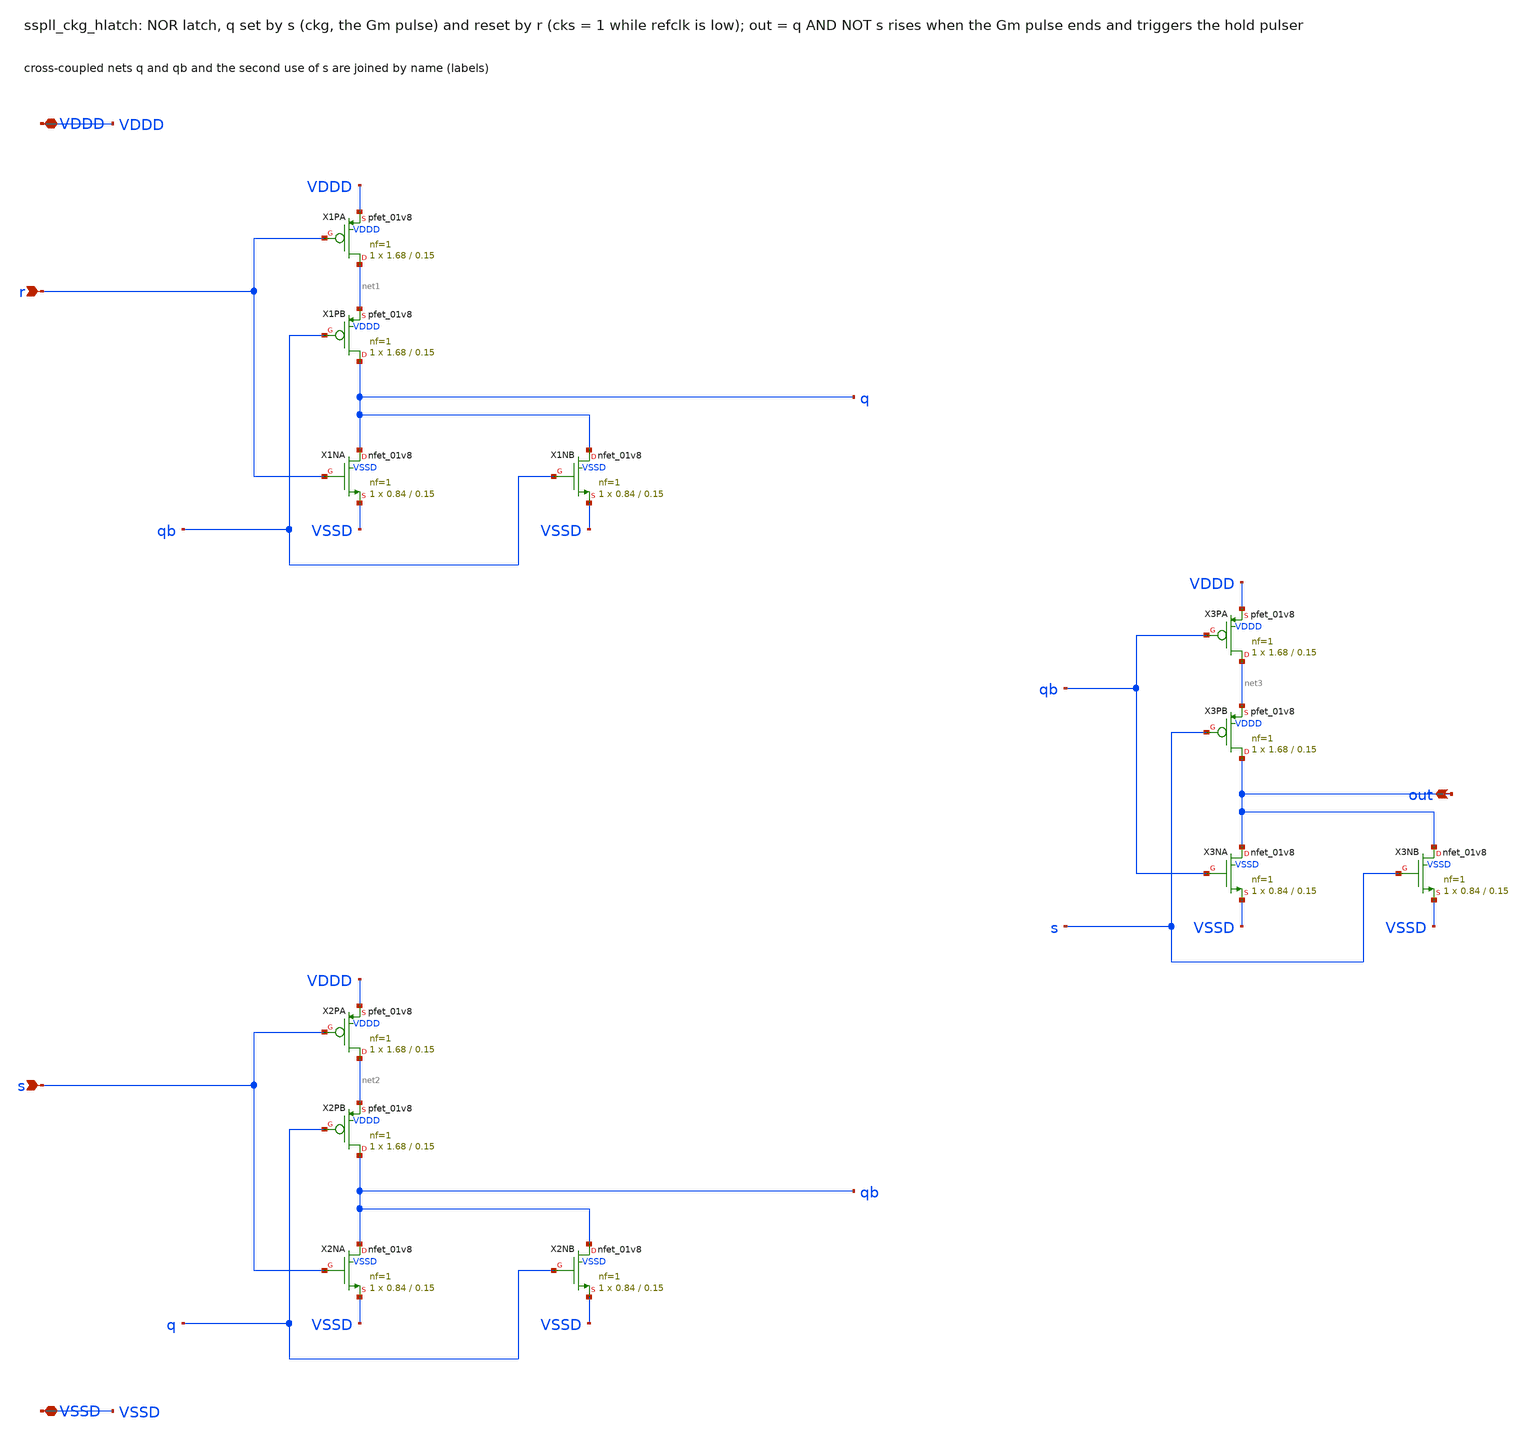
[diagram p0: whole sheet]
** sch_path: xschem/clkgen_hv/sspll_ckg_hlatch.sch
**.subckt sspll_ckg_hlatch r s out VDDD VSSD
*.ipin r
*.ipin s
*.opin out
*.iopin VDDD
*.iopin VSSD
XX1PA net1 r VDDD VDDD sky130_fd_pr__pfet_01v8 L=0.15 W=1.68 nf=1 ad='int((nf+1)/2) * W/nf * 0.29' as='int((nf+2)/2) * W/nf * 0.29'
+ pd='2*int((nf+1)/2) * (W/nf + 0.29)' ps='2*int((nf+2)/2) * (W/nf + 0.29)' nrd='0.29 / W' nrs='0.29 / W'
+ sa=0 sb=0 sd=0 mult=1 m=1
XX1PB q qb net1 VDDD sky130_fd_pr__pfet_01v8 L=0.15 W=1.68 nf=1 ad='int((nf+1)/2) * W/nf * 0.29' as='int((nf+2)/2) * W/nf * 0.29'
+ pd='2*int((nf+1)/2) * (W/nf + 0.29)' ps='2*int((nf+2)/2) * (W/nf + 0.29)' nrd='0.29 / W' nrs='0.29 / W'
+ sa=0 sb=0 sd=0 mult=1 m=1
XX1NA q r VSSD VSSD sky130_fd_pr__nfet_01v8 L=0.15 W=0.84 nf=1 ad='int((nf+1)/2) * W/nf * 0.29' as='int((nf+2)/2) * W/nf * 0.29'
+ pd='2*int((nf+1)/2) * (W/nf + 0.29)' ps='2*int((nf+2)/2) * (W/nf + 0.29)' nrd='0.29 / W' nrs='0.29 / W'
+ sa=0 sb=0 sd=0 mult=1 m=1
XX1NB q qb VSSD VSSD sky130_fd_pr__nfet_01v8 L=0.15 W=0.84 nf=1 ad='int((nf+1)/2) * W/nf * 0.29' as='int((nf+2)/2) * W/nf * 0.29'
+ pd='2*int((nf+1)/2) * (W/nf + 0.29)' ps='2*int((nf+2)/2) * (W/nf + 0.29)' nrd='0.29 / W' nrs='0.29 / W'
+ sa=0 sb=0 sd=0 mult=1 m=1
XX2PA net2 s VDDD VDDD sky130_fd_pr__pfet_01v8 L=0.15 W=1.68 nf=1 ad='int((nf+1)/2) * W/nf * 0.29' as='int((nf+2)/2) * W/nf * 0.29'
+ pd='2*int((nf+1)/2) * (W/nf + 0.29)' ps='2*int((nf+2)/2) * (W/nf + 0.29)' nrd='0.29 / W' nrs='0.29 / W'
+ sa=0 sb=0 sd=0 mult=1 m=1
XX2PB qb q net2 VDDD sky130_fd_pr__pfet_01v8 L=0.15 W=1.68 nf=1 ad='int((nf+1)/2) * W/nf * 0.29' as='int((nf+2)/2) * W/nf * 0.29'
+ pd='2*int((nf+1)/2) * (W/nf + 0.29)' ps='2*int((nf+2)/2) * (W/nf + 0.29)' nrd='0.29 / W' nrs='0.29 / W'
+ sa=0 sb=0 sd=0 mult=1 m=1
XX2NA qb s VSSD VSSD sky130_fd_pr__nfet_01v8 L=0.15 W=0.84 nf=1 ad='int((nf+1)/2) * W/nf * 0.29' as='int((nf+2)/2) * W/nf * 0.29'
+ pd='2*int((nf+1)/2) * (W/nf + 0.29)' ps='2*int((nf+2)/2) * (W/nf + 0.29)' nrd='0.29 / W' nrs='0.29 / W'
+ sa=0 sb=0 sd=0 mult=1 m=1
XX2NB qb q VSSD VSSD sky130_fd_pr__nfet_01v8 L=0.15 W=0.84 nf=1 ad='int((nf+1)/2) * W/nf * 0.29' as='int((nf+2)/2) * W/nf * 0.29'
+ pd='2*int((nf+1)/2) * (W/nf + 0.29)' ps='2*int((nf+2)/2) * (W/nf + 0.29)' nrd='0.29 / W' nrs='0.29 / W'
+ sa=0 sb=0 sd=0 mult=1 m=1
XX3PA net3 qb VDDD VDDD sky130_fd_pr__pfet_01v8 L=0.15 W=1.68 nf=1 ad='int((nf+1)/2) * W/nf * 0.29' as='int((nf+2)/2) * W/nf * 0.29'
+ pd='2*int((nf+1)/2) * (W/nf + 0.29)' ps='2*int((nf+2)/2) * (W/nf + 0.29)' nrd='0.29 / W' nrs='0.29 / W'
+ sa=0 sb=0 sd=0 mult=1 m=1
XX3PB out s net3 VDDD sky130_fd_pr__pfet_01v8 L=0.15 W=1.68 nf=1 ad='int((nf+1)/2) * W/nf * 0.29' as='int((nf+2)/2) * W/nf * 0.29'
+ pd='2*int((nf+1)/2) * (W/nf + 0.29)' ps='2*int((nf+2)/2) * (W/nf + 0.29)' nrd='0.29 / W' nrs='0.29 / W'
+ sa=0 sb=0 sd=0 mult=1 m=1
XX3NA out qb VSSD VSSD sky130_fd_pr__nfet_01v8 L=0.15 W=0.84 nf=1 ad='int((nf+1)/2) * W/nf * 0.29' as='int((nf+2)/2) * W/nf * 0.29'
+ pd='2*int((nf+1)/2) * (W/nf + 0.29)' ps='2*int((nf+2)/2) * (W/nf + 0.29)' nrd='0.29 / W' nrs='0.29 / W'
+ sa=0 sb=0 sd=0 mult=1 m=1
XX3NB out s VSSD VSSD sky130_fd_pr__nfet_01v8 L=0.15 W=0.84 nf=1 ad='int((nf+1)/2) * W/nf * 0.29' as='int((nf+2)/2) * W/nf * 0.29'
+ pd='2*int((nf+1)/2) * (W/nf + 0.29)' ps='2*int((nf+2)/2) * (W/nf + 0.29)' nrd='0.29 / W' nrs='0.29 / W'
+ sa=0 sb=0 sd=0 mult=1 m=1
**.ends
.end
